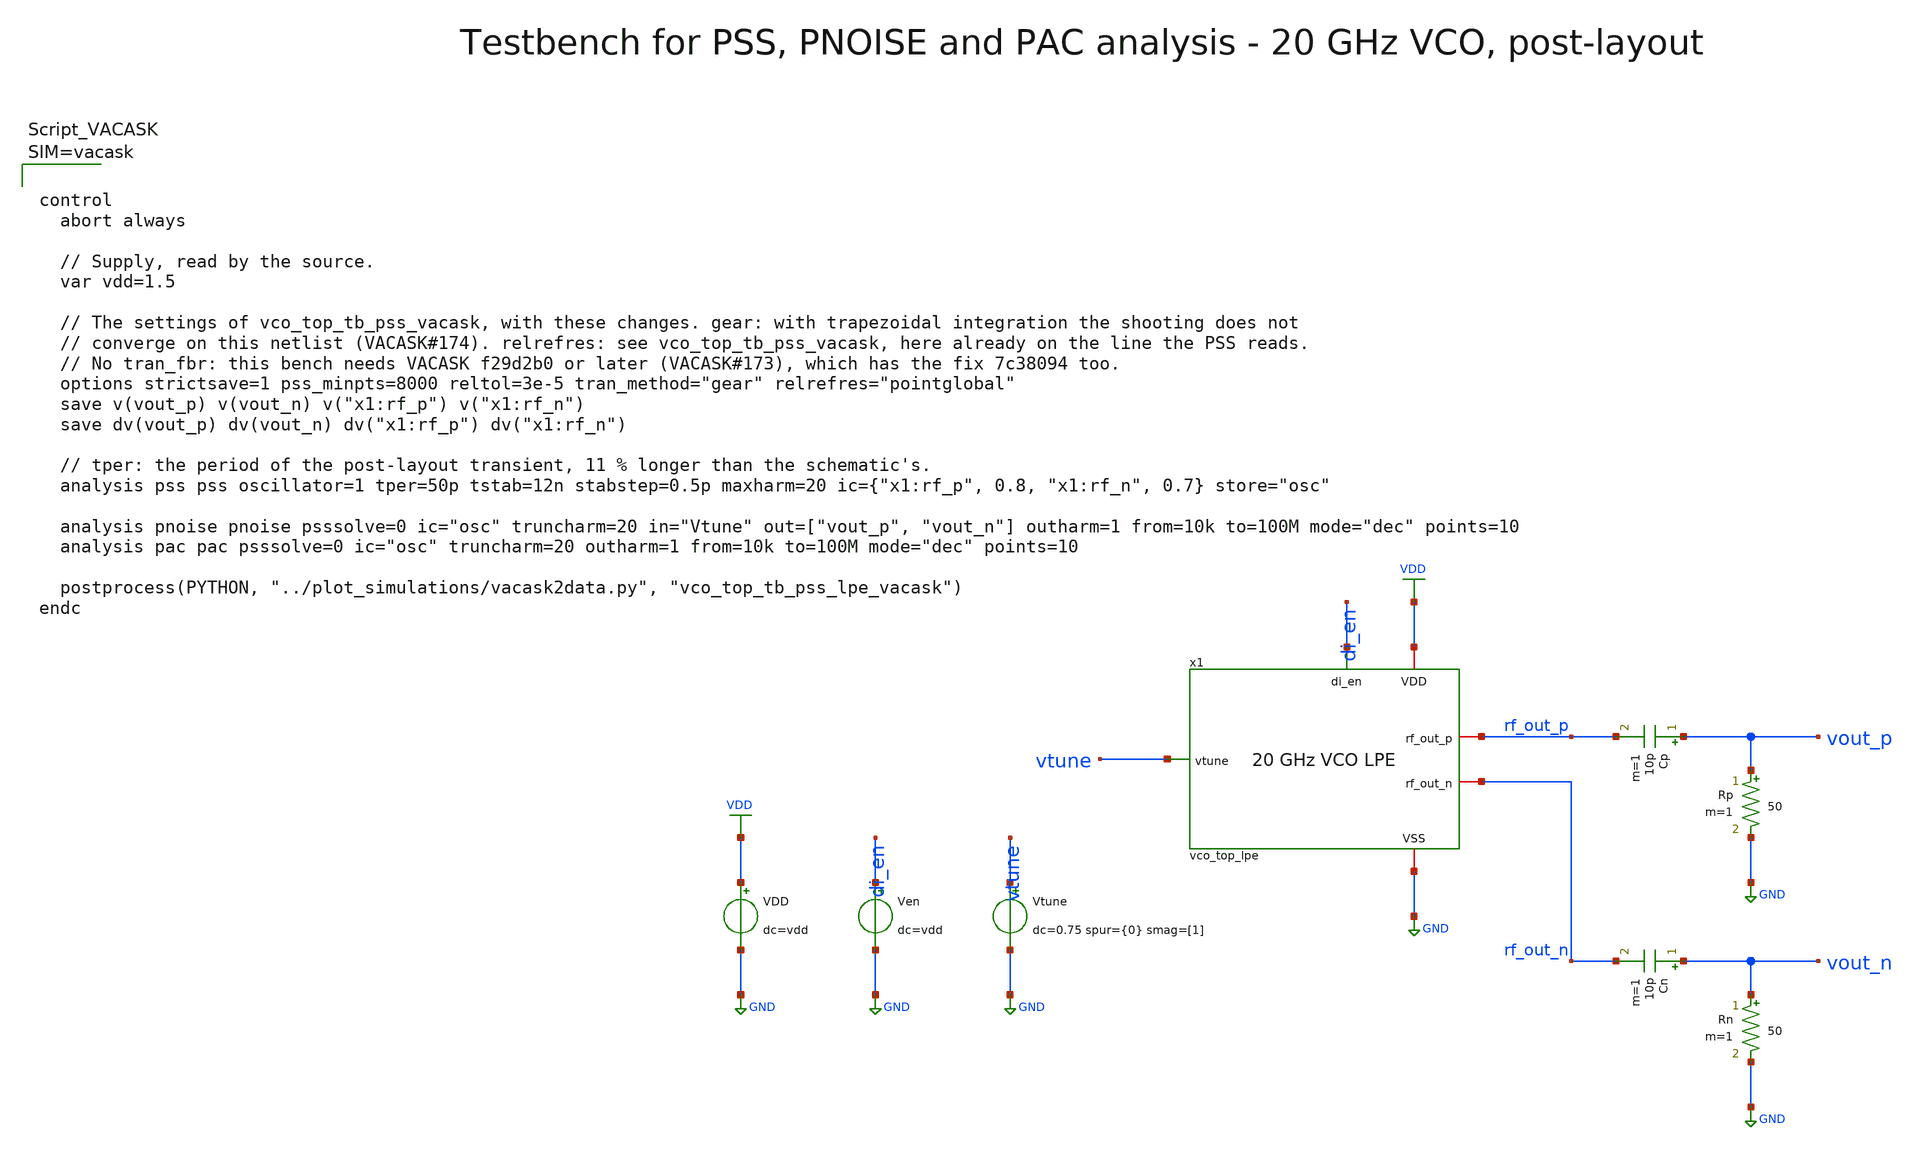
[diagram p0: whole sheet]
** sch_path: macros/vco/testbenches/xschem/vco_top_tb_pss_lpe_vacask.sch
**.subckt vco_top_tb_pss_lpe_vacask
x1 di_en VDD GND vtune rf_out_p rf_out_n vco_top_lpe
Cp vout_p rf_out_p 10p m=1
Rp vout_p GND 50 m=1
Cn vout_n rf_out_n 10p m=1
Rn vout_n GND 50 m=1
VDD VDD GND dc=vdd
Ven di_en GND dc=vdd
Vtune vtune GND dc=0.75 spur={0} smag=[1]
**** begin user architecture code






**** end user architecture code
**.ends

* expanding   symbol:  vco_top_lpe.sym # of pins=6
** sym_path: macros/vco/testbenches/xschem/vco_top_lpe.sym
** sch_path: macros/vco/testbenches/xschem/vco_top_lpe.sch
.subckt vco_top_lpe di_en VDD VSS vtune rf_out_p rf_out_n
*.iopin VDD
*.iopin VSS
*.ipin di_en
*.ipin vtune
*.iopin rf_out_p
*.iopin rf_out_n
xleads di_en vtune VDD VSS rf_out_p rf_out_n rf_p rf_n vdd_core vco_var_rf_p vco_var_rf_n
+ vco_var_VSS vco_top_leads
xind rf_p rf_n vdd_core vco_ind_le
xvar vco_var_rf_p vco_var_rf_n vtune vco_var_VSS vco_var
.ends


* expanding   symbol:  vco_var.sym # of pins=4
** sym_path: macros/vco/schematic/xschem/vco_var.sym
** sch_path: macros/vco/schematic/xschem/vco_var.sch
.subckt vco_var rf_p rf_n vtune VSS
*.ipin vtune
*.iopin rf_p
*.iopin rf_n
*.iopin VSS
XCvar1 rf_p vtune rf_n VSS sg13_hv_svaricap w=3.74u l=0.3u Nx=7 mm_ok=1
XCvar2 rf_p vtune rf_n VSS sg13_hv_svaricap w=3.74u l=0.3u Nx=7 mm_ok=1
XCvar3 rf_p vtune rf_n VSS sg13_hv_svaricap w=3.74u l=0.3u Nx=7 mm_ok=1
.ends

.GLOBAL VDD
.GLOBAL GND
.end
